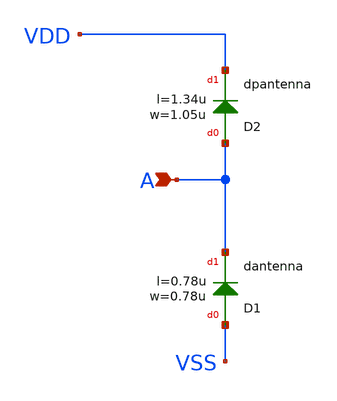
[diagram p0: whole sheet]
** sch_path: ihp-sg13g2/libs.ref/sg13g2_stdcell/sch/xschem/sg13g2_antennanp.sch
* Copyright 2023 IHP PDK Authors
* Licensed under the Apache License, Version 2.0 (the "License");
* you may not use this file except in compliance with the License.
* You may obtain a copy of the License at
* https://www.apache.org/licenses/LICENSE-2.0
* Unless required by applicable law or agreed to in writing, software
* distributed under the License is distributed on an "AS IS" BASIS,
* WITHOUT WARRANTIES OR CONDITIONS OF ANY KIND, either express or implied.
* See the License for the specific language governing permissions and
* limitations under the License.
**.subckt sg13g2_antennanp A
*.ipin A
XD1 VSS A dantenna l=0.78u w=0.78u
XD2 A VDD dpantenna l=1.34u w=1.05u
**.ends
.end
